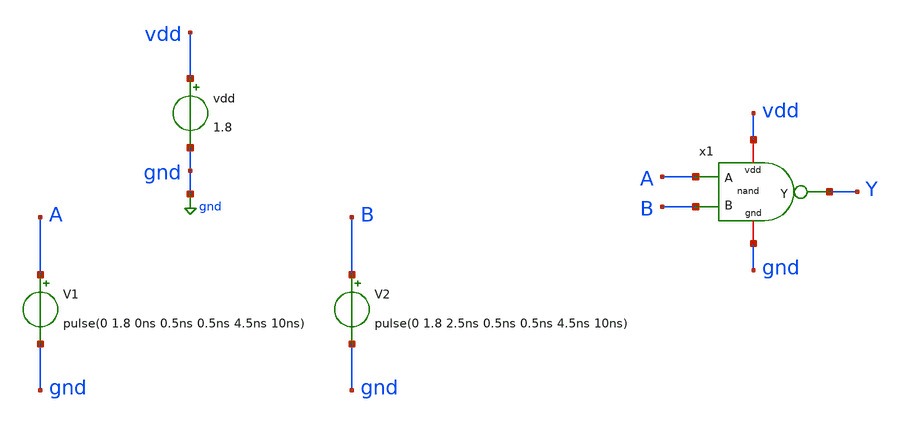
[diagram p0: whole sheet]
** sch_path: LogicGates/nand_tb.sch
**.subckt nand_tb
x1 vdd gnd A B Y nand
vdd vdd gnd 1.8
V1 A gnd pulse(0 1.8 0ns 0.5ns 0.5ns 4.5ns 10ns)
V2 B gnd pulse(0 1.8 2.5ns 0.5ns 0.5ns 4.5ns 10ns)
**** begin user architecture code


.lib /usr/local/share/pdk/sky130A/libs.tech/ngspice/sky130.lib.spice tt
.control
    tran 0.1n 100n
    plot A B
    plot Y
.endc

.save all

**** end user architecture code
**.ends

* expanding   symbol:  LogicGates/nand.sym # of pins=5
** sym_path: LogicGates/nand.sym
** sch_path: LogicGates/nand.sch
.subckt nand vdd gnd A B Y
*.ipin A
*.ipin B
*.iopin vdd
*.iopin gnd
*.opin Y
XM1 Y A net1 gnd sky130_fd_pr__nfet_01v8 L=0.15 W=1 nf=1 ad='int((nf+1)/2) * W/nf * 0.29' as='int((nf+2)/2) * W/nf * 0.29'
+ pd='2*int((nf+1)/2) * (W/nf + 0.29)' ps='2*int((nf+2)/2) * (W/nf + 0.29)' nrd='0.29 / W' nrs='0.29 / W'
+ sa=0 sb=0 sd=0 mult=1 m=1
XM2 net1 B gnd gnd sky130_fd_pr__nfet_01v8 L=0.15 W=1 nf=1 ad='int((nf+1)/2) * W/nf * 0.29' as='int((nf+2)/2) * W/nf * 0.29'
+ pd='2*int((nf+1)/2) * (W/nf + 0.29)' ps='2*int((nf+2)/2) * (W/nf + 0.29)' nrd='0.29 / W' nrs='0.29 / W'
+ sa=0 sb=0 sd=0 mult=1 m=1
XM3 Y A vdd vdd sky130_fd_pr__pfet_01v8 L=0.15 W=2 nf=1 ad='int((nf+1)/2) * W/nf * 0.29' as='int((nf+2)/2) * W/nf * 0.29'
+ pd='2*int((nf+1)/2) * (W/nf + 0.29)' ps='2*int((nf+2)/2) * (W/nf + 0.29)' nrd='0.29 / W' nrs='0.29 / W'
+ sa=0 sb=0 sd=0 mult=1 m=1
XM4 Y B vdd vdd sky130_fd_pr__pfet_01v8 L=0.15 W=2 nf=1 ad='int((nf+1)/2) * W/nf * 0.29' as='int((nf+2)/2) * W/nf * 0.29'
+ pd='2*int((nf+1)/2) * (W/nf + 0.29)' ps='2*int((nf+2)/2) * (W/nf + 0.29)' nrd='0.29 / W' nrs='0.29 / W'
+ sa=0 sb=0 sd=0 mult=1 m=1
.ends

.GLOBAL gnd
.end
